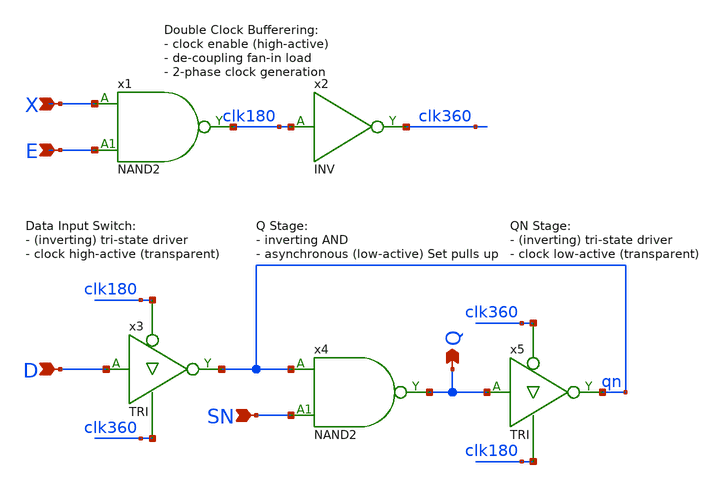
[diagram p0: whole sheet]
** sch_path: Sources/crafted/LATPES.sch
**.subckt LATPES X D Q E SN
*.ipin X
*.ipin D
*.opin Q
*.ipin E
*.ipin SN
x3 D clk180 clk360 qn VDD GND TRI Wmin=1.5u Lmin=1u g=2 m=1
x5 Q clk360 clk180 qn VDD GND TRI Wmin=1.5u Lmin=1u g=2 m=1
x4 qn SN Q VDD GND NAND2 Wmin=1.5u Lmin=1u g=2 m=1
x2 clk180 clk360 VDD GND INV Wmin=1.5u Lmin=1u g=2 m=1
x1 X E clk180 VDD GND NAND2 Wmin=1.5u Lmin=1u g=2 m=1
**.ends
.end
